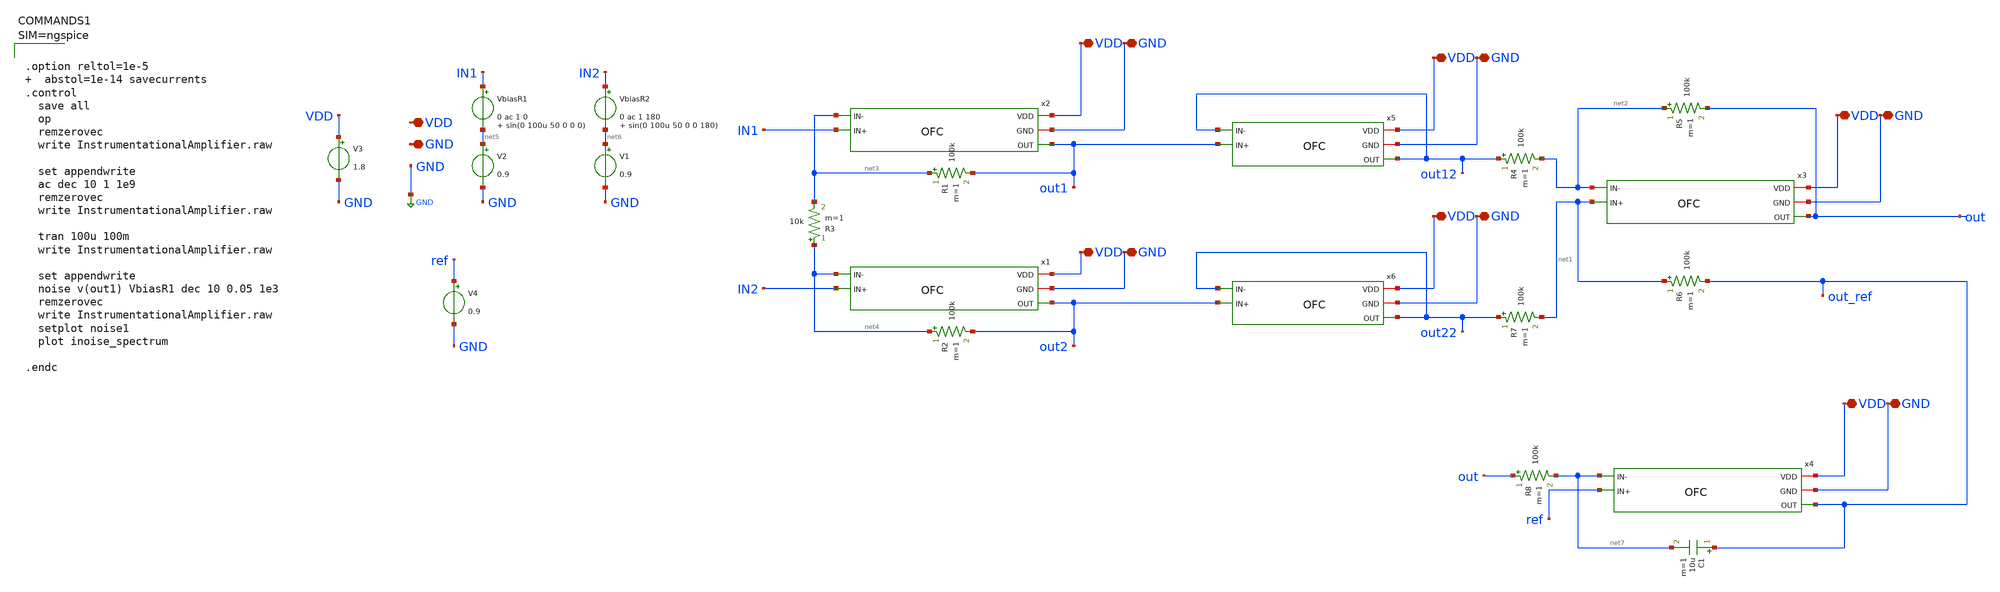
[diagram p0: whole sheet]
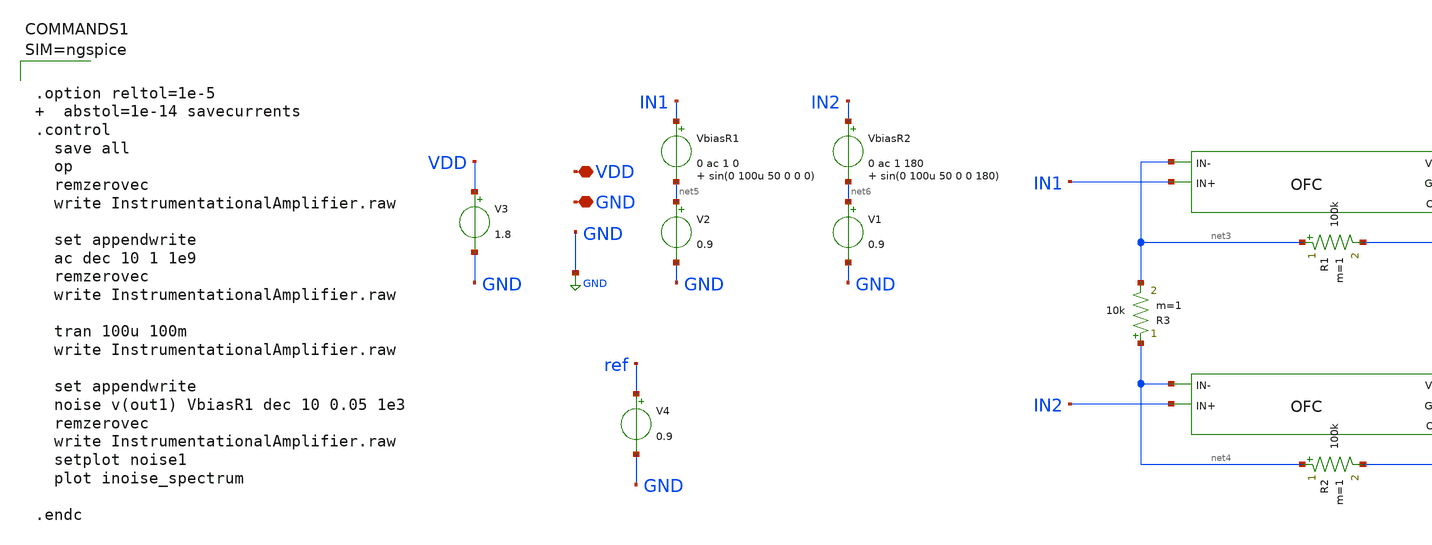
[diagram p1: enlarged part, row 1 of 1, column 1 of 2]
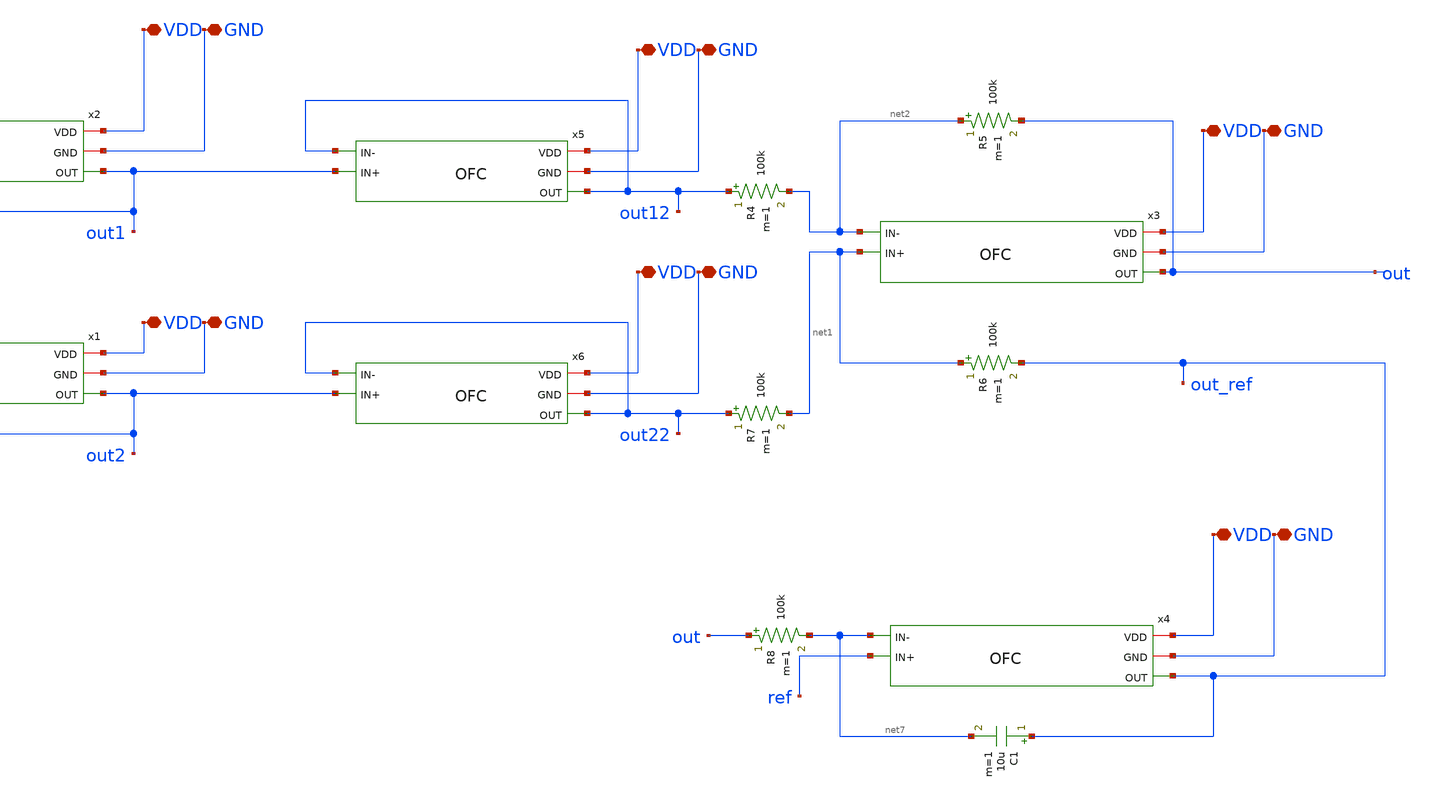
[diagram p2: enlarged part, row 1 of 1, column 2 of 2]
** sch_path: xschem/InstrumentationalAmplifier.sch
**.subckt InstrumentationalAmplifier VDD GND VDD VDD GND GND VDD GND VDD GND VDD GND VDD GND
*.iopin VDD
*.iopin GND
*.iopin VDD
*.iopin VDD
*.iopin GND
*.iopin GND
*.iopin VDD
*.iopin GND
*.iopin VDD
*.iopin GND
*.iopin VDD
*.iopin GND
*.iopin VDD
*.iopin GND
x1 VDD GND out2 net4 IN2 OFC
x2 VDD GND out1 net3 IN1 OFC
x3 VDD GND out net2 net1 OFC
V3 VDD GND 1.8
VbiasR1 IN1 net5 0 ac 1 0 sin(0 100u 50 0 0 0)
V2 net5 GND 0.9
VbiasR2 IN2 net6 0 ac 1 180 sin(0 100u 50 0 0 180)
V1 net6 GND 0.9
R1 net3 out1 100k m=1
R2 net4 out2 100k m=1
R3 net4 net3 10k m=1
V4 ref GND 0.9
x4 VDD GND out_ref net7 ref OFC
R6 net1 out_ref 100k m=1
R8 out net7 100k m=1
C1 out_ref net7 10u m=1
R5 net2 out 100k m=1
x5 VDD GND out12 out12 out1 OFC
x6 VDD GND out22 out22 out2 OFC
R4 out12 net2 100k m=1
R7 out22 net1 100k m=1
**** begin user architecture code



.option reltol=1e-5   abstol=1e-14 savecurrents
.control
  save all
  op
  remzerovec
  write InstrumentationalAmplifier.raw

  set appendwrite
  ac dec 10 1 1e9
  remzerovec
  write InstrumentationalAmplifier.raw

  tran 100u 100m
  write InstrumentationalAmplifier.raw

  set appendwrite
  noise v(out1) VbiasR1 dec 10 0.05 1e3
  remzerovec
  write InstrumentationalAmplifier.raw
  setplot noise1
  plot inoise_spectrum

.endc



.lib $::SKYWATER_MODELS/sky130.lib.spice tt
**** end user architecture code
**.ends

* expanding   symbol:  OFC.sym # of pins=5
** sym_path: OFC.sym
** sch_path: OFC.sch
.subckt OFC VDD GND OUT IN- IN+
*.iopin VDD
*.iopin GND
*.ipin IN+
*.ipin IN-
*.opin OUT
XM11 S Vb VDD VDD sky130_fd_pr__pfet_01v8_lvt L=1 W=60 nf=2 ad='int((nf+1)/2) * W/nf * 0.29' as='int((nf+2)/2) * W/nf * 0.29'
+ pd='2*int((nf+1)/2) * (W/nf + 0.29)' ps='2*int((nf+2)/2) * (W/nf + 0.29)' nrd='0.29 / W' nrs='0.29 / W'
+ sa=0 sb=0 sd=0 mult=2 m=2
XM1 D1 IN+ S S sky130_fd_pr__pfet_01v8_lvt L=10 W=25 nf=2 ad='int((nf+1)/2) * W/nf * 0.29' as='int((nf+2)/2) * W/nf * 0.29'
+ pd='2*int((nf+1)/2) * (W/nf + 0.29)' ps='2*int((nf+2)/2) * (W/nf + 0.29)' nrd='0.29 / W' nrs='0.29 / W'
+ sa=0 sb=0 sd=0 mult=2 m=2
XM2 D2 IN- S S sky130_fd_pr__pfet_01v8_lvt L=10 W=25 nf=2 ad='int((nf+1)/2) * W/nf * 0.29' as='int((nf+2)/2) * W/nf * 0.29'
+ pd='2*int((nf+1)/2) * (W/nf + 0.29)' ps='2*int((nf+2)/2) * (W/nf + 0.29)' nrd='0.29 / W' nrs='0.29 / W'
+ sa=0 sb=0 sd=0 mult=2 m=2
XM3 OUT Vc1 D2 GND sky130_fd_pr__nfet_01v8_lvt L=1 W=4 nf=1 ad='int((nf+1)/2) * W/nf * 0.29' as='int((nf+2)/2) * W/nf * 0.29'
+ pd='2*int((nf+1)/2) * (W/nf + 0.29)' ps='2*int((nf+2)/2) * (W/nf + 0.29)' nrd='0.29 / W' nrs='0.29 / W'
+ sa=0 sb=0 sd=0 mult=1 m=1
XM4 D2 Vc GND GND sky130_fd_pr__nfet_01v8_lvt L=1 W=2.8 nf=1 ad='int((nf+1)/2) * W/nf * 0.29' as='int((nf+2)/2) * W/nf * 0.29'
+ pd='2*int((nf+1)/2) * (W/nf + 0.29)' ps='2*int((nf+2)/2) * (W/nf + 0.29)' nrd='0.29 / W' nrs='0.29 / W'
+ sa=0 sb=0 sd=0 mult=1 m=1
XM5 D1 Vc GND GND sky130_fd_pr__nfet_01v8_lvt L=1 W=2.8 nf=1 ad='int((nf+1)/2) * W/nf * 0.29' as='int((nf+2)/2) * W/nf * 0.29'
+ pd='2*int((nf+1)/2) * (W/nf + 0.29)' ps='2*int((nf+2)/2) * (W/nf + 0.29)' nrd='0.29 / W' nrs='0.29 / W'
+ sa=0 sb=0 sd=0 mult=1 m=1
XM6 G Vc1 D1 GND sky130_fd_pr__nfet_01v8_lvt L=1 W=4 nf=1 ad='int((nf+1)/2) * W/nf * 0.29' as='int((nf+2)/2) * W/nf * 0.29'
+ pd='2*int((nf+1)/2) * (W/nf + 0.29)' ps='2*int((nf+2)/2) * (W/nf + 0.29)' nrd='0.29 / W' nrs='0.29 / W'
+ sa=0 sb=0 sd=0 mult=1 m=1
XM7 G Vc2 D9 D9 sky130_fd_pr__pfet_01v8_lvt L=2.23 W=3 nf=1 ad='int((nf+1)/2) * W/nf * 0.29' as='int((nf+2)/2) * W/nf * 0.29'
+ pd='2*int((nf+1)/2) * (W/nf + 0.29)' ps='2*int((nf+2)/2) * (W/nf + 0.29)' nrd='0.29 / W' nrs='0.29 / W'
+ sa=0 sb=0 sd=0 mult=1 m=1
XM9 D9 G VDD VDD sky130_fd_pr__pfet_01v8_lvt L=2.23 W=4 nf=1 ad='int((nf+1)/2) * W/nf * 0.29' as='int((nf+2)/2) * W/nf * 0.29'
+ pd='2*int((nf+1)/2) * (W/nf + 0.29)' ps='2*int((nf+2)/2) * (W/nf + 0.29)' nrd='0.29 / W' nrs='0.29 / W'
+ sa=0 sb=0 sd=0 mult=1 m=1
XM8 D10 G VDD VDD sky130_fd_pr__pfet_01v8_lvt L=2.23 W=4 nf=1 ad='int((nf+1)/2) * W/nf * 0.29' as='int((nf+2)/2) * W/nf * 0.29'
+ pd='2*int((nf+1)/2) * (W/nf + 0.29)' ps='2*int((nf+2)/2) * (W/nf + 0.29)' nrd='0.29 / W' nrs='0.29 / W'
+ sa=0 sb=0 sd=0 mult=1 m=1
XM10 OUT Vc2 D10 D10 sky130_fd_pr__pfet_01v8_lvt L=2.23 W=3 nf=1 ad='int((nf+1)/2) * W/nf * 0.29' as='int((nf+2)/2) * W/nf * 0.29'
+ pd='2*int((nf+1)/2) * (W/nf + 0.29)' ps='2*int((nf+2)/2) * (W/nf + 0.29)' nrd='0.29 / W' nrs='0.29 / W'
+ sa=0 sb=0 sd=0 mult=1 m=1
XR2 Vb VDD GND sky130_fd_pr__res_xhigh_po_0p35 L=5 mult=1 m=1
XR3 GND Vb GND sky130_fd_pr__res_xhigh_po_0p35 L=13.2 mult=1 m=1
XR1 Vc VDD GND sky130_fd_pr__res_xhigh_po_0p35 L=5 mult=1 m=1
XR4 GND Vc GND sky130_fd_pr__res_xhigh_po_0p35 L=3.07 mult=1 m=1
XR5 Vc1 VDD GND sky130_fd_pr__res_xhigh_po_0p35 L=5 mult=1 m=1
XR6 GND Vc1 GND sky130_fd_pr__res_xhigh_po_0p35 L=13.2 mult=1 m=1
XR7 Vc2 VDD GND sky130_fd_pr__res_xhigh_po_0p35 L=5 mult=1 m=1
XR8 GND Vc2 GND sky130_fd_pr__res_xhigh_po_0p35 L=1.6 mult=1 m=1
.ends

.GLOBAL GND
.end
